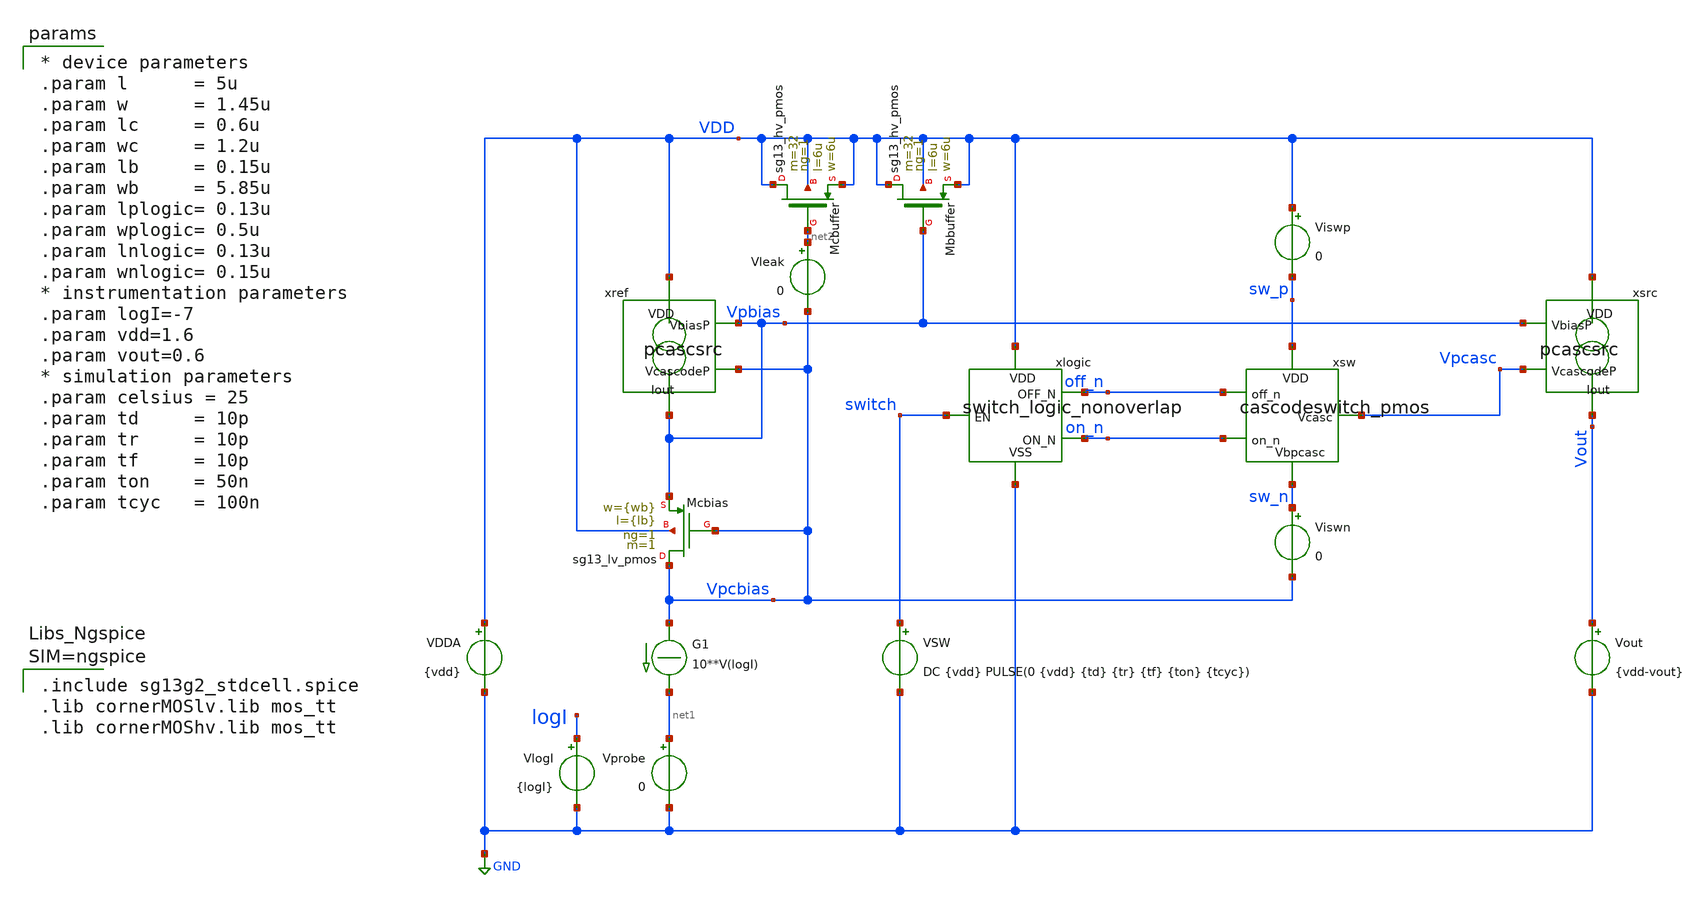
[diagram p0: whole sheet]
** sch_path: xschem/test_switchedsources_tran.sch
**.subckt test_switchedsources_tran
Vout Vout GND {vdd-vout}
.save i(vout)
Vprobe net1 GND 0
.save i(vprobe)
G1 Vpcbias net1 CUR=' 10**V(logI) '
VlogI logI GND {logI}
.save i(vlogi)
xref VDD Vpbias Vpcbias Vpbias pcascsrc l={l} w={w} lc={lc} wc={wc}
xsrc VDD Vpbias Vpcasc Vout pcascsrc l={l} w={w} lc={lc} wc={wc}
VDDA VDD GND {vdd}
.save i(vdda)
XMcbias Vpcbias Vpcbias Vpbias VDD sg13_lv_pmos w={wb} l={lb} ng=1 m=1 mm_ok=1
xsw sw_p off_n Vpcasc on_n sw_n cascodeswitch_pmos
xlogic VDD off_n switch on_n GND switch_logic_nonoverlap lenp=0.13u wp=0.5u lenn=0.13u wn=0.15u
VSW switch GND DC {vdd} PULSE(0 {vdd} {td} {tr} {tf} {ton} {tcyc})
.save i(vsw)
Viswp VDD sw_p 0
.save i(viswp)
Viswn sw_n Vpcbias 0
.save i(viswn)
XMcbuffer VDD net2 VDD VDD sg13_hv_pmos w=6u l=6u ng=1 m=32 mm_ok=1
XMbbuffer VDD Vpbias VDD VDD sg13_hv_pmos w=6u l=6u ng=1 m=32 mm_ok=1
Vleak net2 Vpcbias 0
.save i(vleak)
**** begin user architecture code


.include test_switchedsources_tran.save
.temp=27
.options gmin=1e-15 abstol=1p method=gear
.options savecurrents
.control
save all
op
write test_switchedsources_tran.raw
set appendwrite
*dc Vout 0 1.6 10m VlogI -8 -6 0.5
tran 10p 500n
write test_switchedsources_tran.raw
plot 2*(vout#branch-vprobe#branch)/(vprobe#branch+vout#branch)
plot vdd vpbias vpcbias switch on_n off_n vpcasc vout xref.drain xsrc.drain
plot vout#branch vprobe#branch
plot switch on_n off_n Vpcasc
*plot @n.xsw.xmbias.nsg13_lv_pmos[ids] @n.xsw.xmpullup.nsg13_lv_pmos[ids]
plot viswp#branch viswn#branch
plot 0.5*(viswp#branch+viswn#branch) viswp#branch-viswn#branch
.endc




.include sg13g2_stdcell.spice
.lib cornerMOSlv.lib mos_tt
.lib cornerMOShv.lib mos_tt



* device parameters
.param l      = 5u
.param w      = 1.45u
.param lc     = 0.6u
.param wc     = 1.2u
.param lb     = 0.15u
.param wb     = 5.85u
.param lplogic= 0.13u
.param wplogic= 0.5u
.param lnlogic= 0.13u
.param wnlogic= 0.15u
* instrumentation parameters
.param logI=-7
.param vdd=1.6
.param vout=0.6
* simulation parameters
.param celsius = 25
.param td     = 10p
.param tr     = 10p
.param tf     = 10p
.param ton    = 50n
.param tcyc   = 100n


**** end user architecture code
**.ends

* expanding   symbol:  pcascsrc.sym # of pins=4
** sym_path: xschem/pcascsrc.sym
** sch_path: xschem/pcascsrc.sch
.subckt pcascsrc VDD VbiasP VcascodeP Iout  l=2u w=.74u lc=.3u wc=.3u
*.ipin VcascodeP
*.ipin VbiasP
*.opin Iout
*.ipin VDD
XMsrc drain VbiasP VDD VDD sg13_lv_pmos w={w} l={l} ng=1 m=1 mm_ok=1
XMcasc Iout VcascodeP drain VDD sg13_lv_pmos w={wc} l={lc} ng=1 m=1 mm_ok=1
.ends


* expanding   symbol:  cascodeswitch_pmos.sym # of pins=5
** sym_path: xschem/cascodeswitch_pmos.sym
** sch_path: xschem/cascodeswitch_pmos.sch
.subckt cascodeswitch_pmos VDD off_n Vcasc on_n Vbpcasc
*.ipin off_n
*.ipin Vbpcasc
*.opin Vcasc
*.ipin on_n
*.ipin VDD
XMpullup Vcasc off_n VDD VDD sg13_lv_pmos w=0.3u l=0.13u ng=1 m=1 mm_ok=1
XMbias Vbpcasc on_n Vcasc VDD sg13_lv_pmos w=0.3u l=0.13u ng=1 m=1 mm_ok=1
.ends


* expanding   symbol:  switch_logic_nonoverlap.sym # of pins=5
** sym_path: xschem/switch_logic_nonoverlap.sym
** sch_path: xschem/switch_logic_nonoverlap.sch
.subckt switch_logic_nonoverlap VDD OFF_N EN ON_N VSS  lenp=0.13u wp=0.5u lenn=0.13u wn=0.15u
*.iopin VSS
*.iopin VDD
*.ipin EN
*.opin ON_N
*.opin OFF_N
x0 EN_N EN VDD VSS sg13g2_inv_1
x1 EN_P EN_N VDD VSS sg13g2_inv_1
xnonoverlap VDD VSS EN_P EN_N ON_N OFF_N nonoverlap
.ends


* expanding   symbol:  sg13g2_stdcells/sg13g2_inv_1.sym # of pins=2
** sym_path: sg13g2_stdcells/sg13g2_inv_1.sym
** sch_path: sg13g2_stdcells/sg13g2_inv_1.sch
.subckt sg13g2_inv_1 Y A VDD VSS
*.opin Y
*.ipin A
*.iopin VDD
*.iopin VSS
XM1 Y A VSS VSS sg13_lv_nmos w=740.00n l=130.00n ng=1 m=1 mm_ok=1
XM2 Y A VDD VDD sg13_lv_pmos w=1.12u l=130.00n ng=1 m=1 mm_ok=1
.ends


* expanding   symbol:  nonoverlap.sym # of pins=6
** sym_path: xschem/nonoverlap.sym
** sch_path: xschem/nonoverlap.sch
.subckt nonoverlap VDD VSS INP INN OUTN OUTP
*.iopin VSS
*.iopin VDD
*.ipin INP
*.ipin INN
*.opin OUTP
*.opin OUTN
XM1 OUTN INP VDD VDD sg13_lv_pmos w=0.3u l=0.13u ng=1 m=1 mm_ok=1
XM2 OUTP INN VDD VDD sg13_lv_pmos w=0.3u l=0.13u ng=1 m=1 mm_ok=1
XM3 OUTN OUTP VSS VSS sg13_lv_nmos w=0.15u l=0.52u ng=1 m=1 mm_ok=1
XM4 OUTP OUTN VSS VSS sg13_lv_nmos w=0.15u l=0.52u ng=1 m=1 mm_ok=1
.ends

.GLOBAL GND
.end
